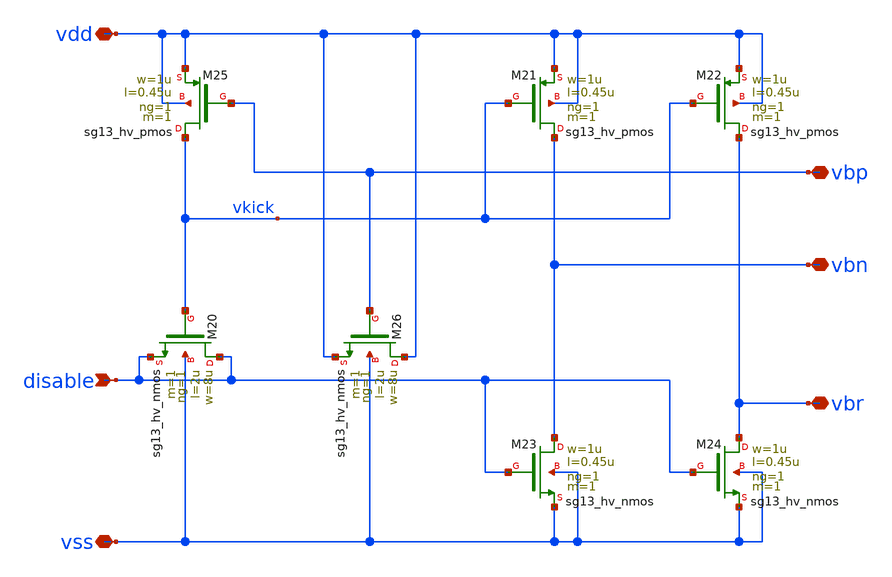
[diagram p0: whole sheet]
** sch_path: sudelbuecher/design_considerations/consolidation/reference_sheets_2026-10-20/macros/OgueyAebischerBias/schematic/xschem/ToBiasStartup.sch
**.subckt ToBiasStartup vss vdd vbp vbn vbr disable
*.iopin vss
*.iopin vdd
*.iopin vbp
*.iopin vbn
*.iopin vbr
*.ipin disable
XM24 vbr disable vss vss sg13_hv_nmos w=1u l=0.45u ng=1 m=1 mm_ok=1
XM22 vbr vkick vdd vdd sg13_hv_pmos w=1u l=0.45u ng=1 m=1 mm_ok=1
XM25 vkick vbp vdd vdd sg13_hv_pmos w=1u l=0.45u ng=1 m=1 mm_ok=1
XM23 vbn disable vss vss sg13_hv_nmos w=1u l=0.45u ng=1 m=1 mm_ok=1
XM21 vbn vkick vdd vdd sg13_hv_pmos w=1u l=0.45u ng=1 m=1 mm_ok=1
XM20 disable vkick disable vss sg13_hv_nmos w=8u l=2u ng=1 m=1 mm_ok=1
XM26 vdd vbp vdd vss sg13_hv_nmos w=8u l=2u ng=1 m=1 mm_ok=1
**.ends
.end
